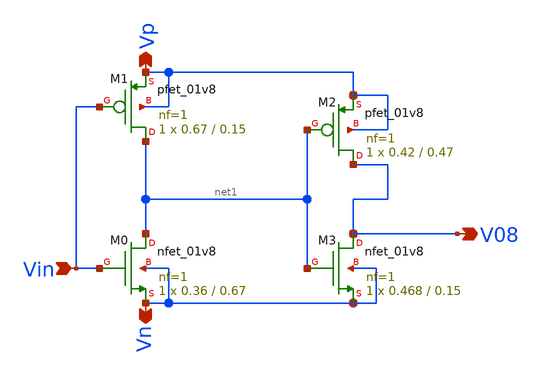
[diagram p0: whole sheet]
** sch_path: xschem/Vth_sch/Symbol/th08_backup.sch
**.subckt th08_backup Vn Vp Vin V08
*.opin Vn
*.opin Vp
*.ipin Vin
*.opin V08
XM2 V08 net1 Vp Vp sky130_fd_pr__pfet_01v8 L=0.47 W=0.42 nf=1 ad='int((nf+1)/2) * W/nf * 0.29' as='int((nf+2)/2) * W/nf * 0.29'
+ pd='2*int((nf+1)/2) * (W/nf + 0.29)' ps='2*int((nf+2)/2) * (W/nf + 0.29)' nrd='0.29 / W' nrs='0.29 / W'
+ sa=0 sb=0 sd=0 mult=1 m=1
XM3 V08 net1 Vn Vn sky130_fd_pr__nfet_01v8 L=0.15 W=0.468 nf=1 ad='int((nf+1)/2) * W/nf * 0.29' as='int((nf+2)/2) * W/nf * 0.29'
+ pd='2*int((nf+1)/2) * (W/nf + 0.29)' ps='2*int((nf+2)/2) * (W/nf + 0.29)' nrd='0.29 / W' nrs='0.29 / W'
+ sa=0 sb=0 sd=0 mult=1 m=1
XM1 net1 Vin Vp Vp sky130_fd_pr__pfet_01v8 L=0.15 W=0.67 nf=1 ad='int((nf+1)/2) * W/nf * 0.29' as='int((nf+2)/2) * W/nf * 0.29'
+ pd='2*int((nf+1)/2) * (W/nf + 0.29)' ps='2*int((nf+2)/2) * (W/nf + 0.29)' nrd='0.29 / W' nrs='0.29 / W'
+ sa=0 sb=0 sd=0 mult=1 m=1
XM0 net1 Vin Vn Vn sky130_fd_pr__nfet_01v8 L=0.67 W=0.36 nf=1 ad='int((nf+1)/2) * W/nf * 0.29' as='int((nf+2)/2) * W/nf * 0.29'
+ pd='2*int((nf+1)/2) * (W/nf + 0.29)' ps='2*int((nf+2)/2) * (W/nf + 0.29)' nrd='0.29 / W' nrs='0.29 / W'
+ sa=0 sb=0 sd=0 mult=1 m=1
**.ends
.end
